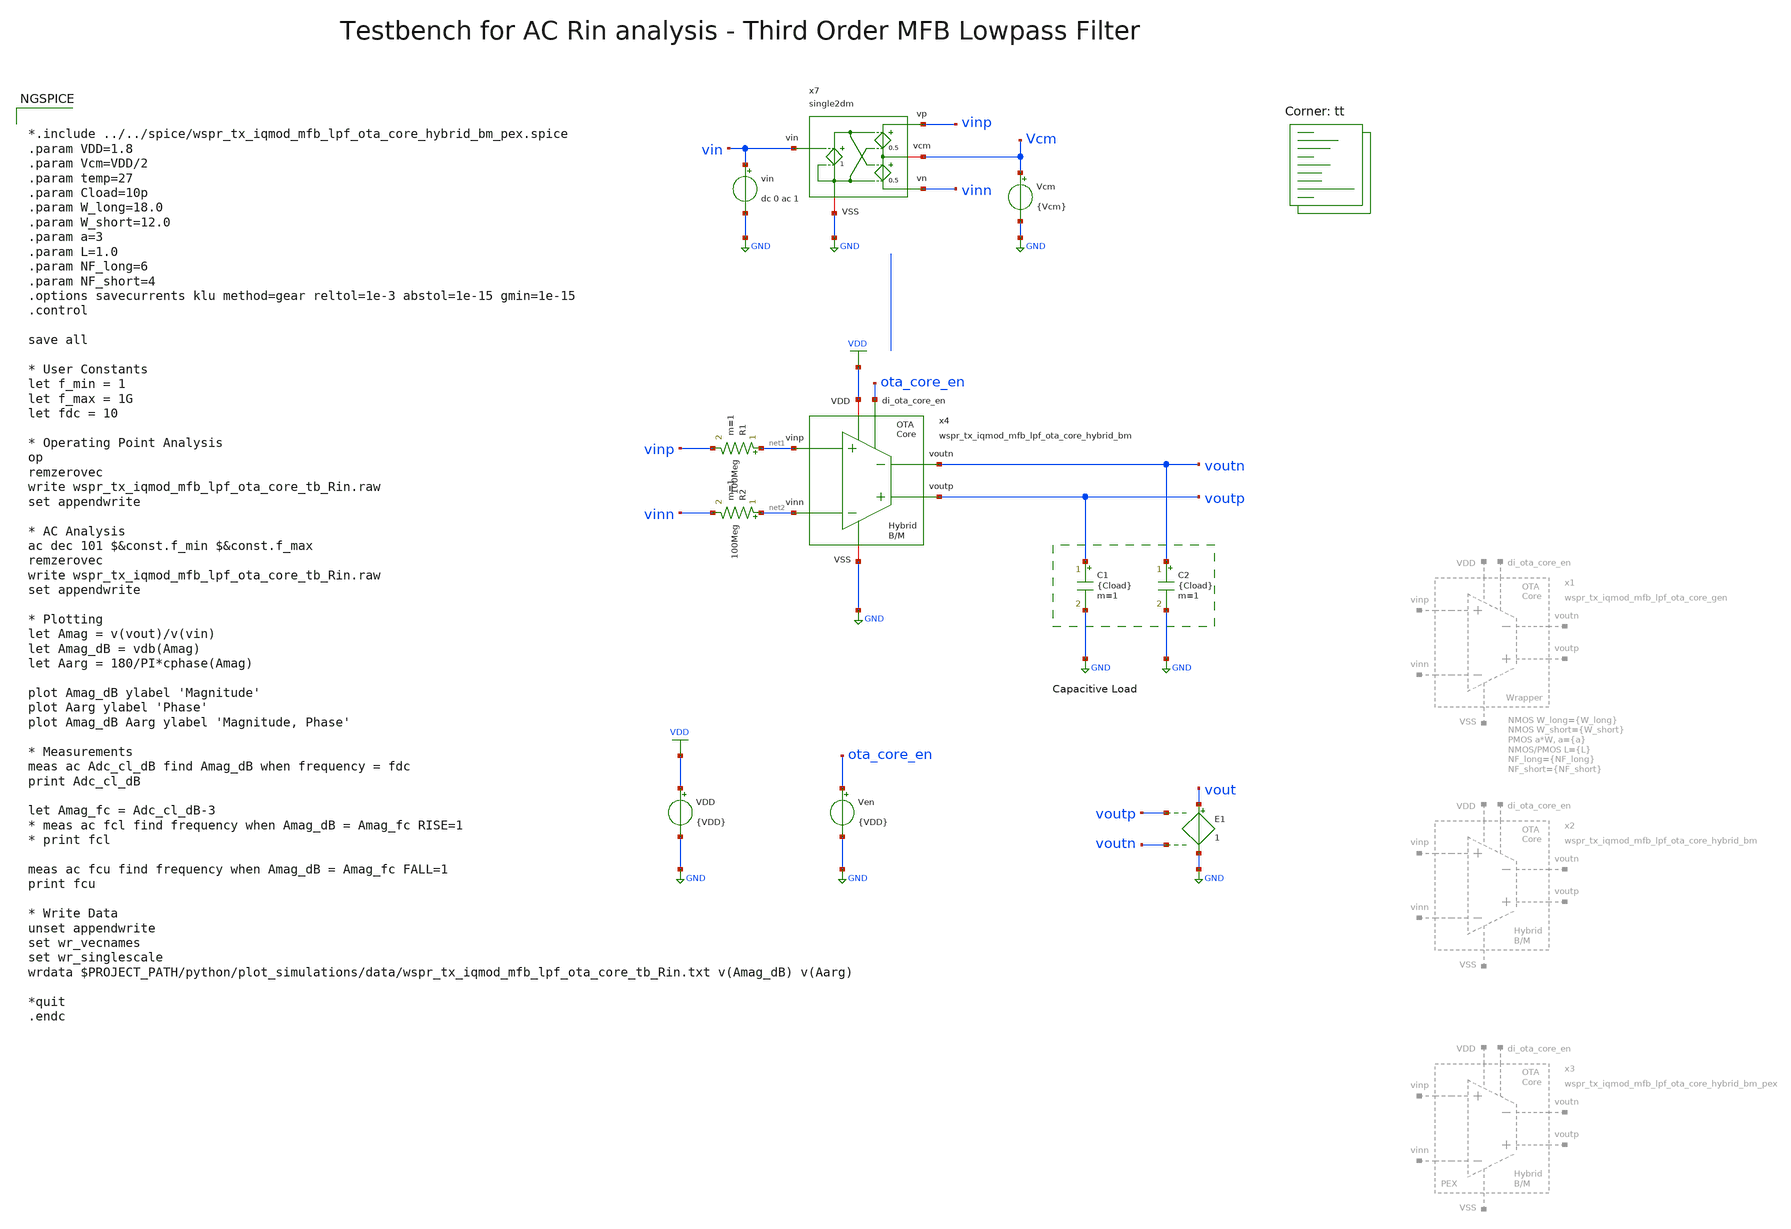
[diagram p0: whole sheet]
** sch_path: sky130/xschem/testbenches/wspr_tx_iqmod_mfb_lpf_ota_core_tb_Rin.sch
**.subckt wspr_tx_iqmod_mfb_lpf_ota_core_tb_Rin
VDD VDD GND {VDD}
Vcm Vcm GND {Vcm}
Ven ota_core_en GND {VDD}
E1 vout GND voutp voutn 1
vin vin GND dc 0 ac 1
R1 net1 vinp 100Meg m=1
R2 net2 vinn 100Meg m=1
C1 voutp GND {Cload} m=1
C2 voutn GND {Cload} m=1
x4 ota_core_en voutp voutn net2 net1 VDD GND wspr_tx_iqmod_mfb_lpf_ota_core_hybrid_bm
x7 vinp vin Vcm GND vinn single2dm
**** begin user architecture code


*.include ../../spice/wspr_tx_iqmod_mfb_lpf_ota_core_hybrid_bm_pex.spice
.param VDD=1.8
.param Vcm=VDD/2
.param temp=27
.param Cload=10p
.param W_long=18.0
.param W_short=12.0
.param a=3
.param L=1.0
.param NF_long=6
.param NF_short=4
.options savecurrents klu method=gear reltol=1e-3 abstol=1e-15 gmin=1e-15
.control

save all

* User Constants
let f_min = 1
let f_max = 1G
let fdc = 10

* Operating Point Analysis
op
remzerovec
write wspr_tx_iqmod_mfb_lpf_ota_core_tb_Rin.raw
set appendwrite

* AC Analysis
ac dec 101 $&const.f_min $&const.f_max
remzerovec
write wspr_tx_iqmod_mfb_lpf_ota_core_tb_Rin.raw
set appendwrite

* Plotting
let Amag = v(vout)/v(vin)
let Amag_dB = vdb(Amag)
let Aarg = 180/PI*cphase(Amag)

plot Amag_dB ylabel 'Magnitude'
plot Aarg ylabel 'Phase'
plot Amag_dB Aarg ylabel 'Magnitude, Phase'

* Measurements
meas ac Adc_cl_dB find Amag_dB when frequency = fdc
print Adc_cl_dB

let Amag_fc = Adc_cl_dB-3
* meas ac fcl find frequency when Amag_dB = Amag_fc RISE=1
* print fcl

meas ac fcu find frequency when Amag_dB = Amag_fc FALL=1
print fcu

* Write Data
unset appendwrite
set wr_vecnames
set wr_singlescale
wrdata $PROJECT_PATH/python/plot_simulations/data/wspr_tx_iqmod_mfb_lpf_ota_core_tb_Rin.txt
+ v(Amag_dB) v(Aarg)

*quit
.endc


.lib $::SKYWATER_MODELS/sky130.lib.spice tt
**** end user architecture code
**.ends
.GLOBAL GND
.GLOBAL VDD
.end
